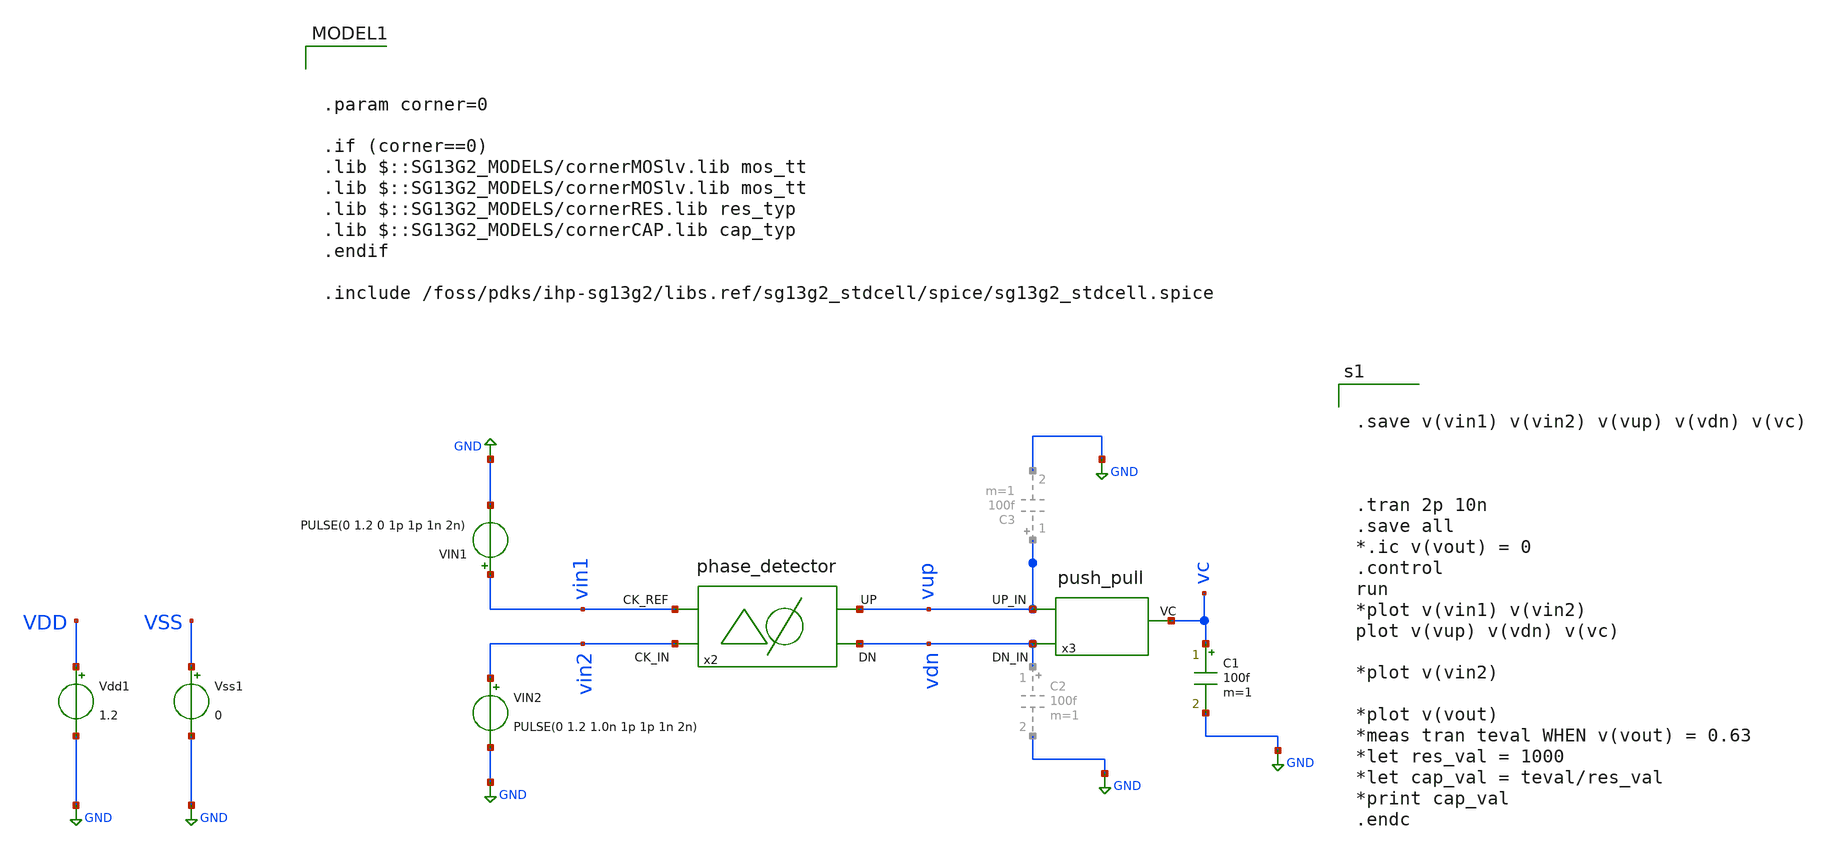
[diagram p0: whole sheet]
** sch_path: sch/phase_detector/tb_QPD.sch
**.subckt tb_QPD
VIN1 vin1 GND PULSE(0 1.2 0 1p 1p 1n 2n)
x2 vin2 vup vin1 vdn phase_detector
VIN2 vin2 GND PULSE(0 1.2 1.0n 1p 1p 1n 2n)
x3 vup vc vdn push_pull
C1 vc GND 100f m=1
Vss1 VSS GND 0
Vdd1 VDD GND 1.2
**** begin user architecture code


.save v(vin1) v(vin2) v(vup) v(vdn) v(vc)



.tran 2p 10n
.save all
*.ic v(vout) = 0
.control
run
*plot v(vin1) v(vin2)
plot v(vup) v(vdn) v(vc)

*plot v(vin2)

*plot v(vout)
*meas tran teval WHEN v(vout) = 0.63
*let res_val = 1000
*let cap_val = teval/res_val
*print cap_val
.endc




.param corner=0

.if (corner==0)
.lib $::SG13G2_MODELS/cornerMOSlv.lib mos_tt
.lib $::SG13G2_MODELS/cornerMOSlv.lib mos_tt
.lib $::SG13G2_MODELS/cornerRES.lib res_typ
.lib $::SG13G2_MODELS/cornerCAP.lib cap_typ
.endif

.include /foss/pdks/ihp-sg13g2/libs.ref/sg13g2_stdcell/spice/sg13g2_stdcell.spice

**** end user architecture code
**.ends
.GLOBAL GND
.end
